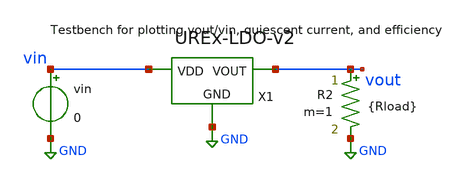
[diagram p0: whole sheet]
** sch_path: xschem/testbenches/VoutvsVin-v2.sch
**.subckt VoutvsVin-v2
vin vin GND 0
R2 vout GND {Rload} m=1
X1 vin vout GND UREx-LDO-v2
**** begin user architecture code



.lib /usr/local/share/pdk/sky130A/libs.tech/ngspice/sky130.lib.spice tt
.param Rload = 20
.dc vin 0.5 5 0.1
*.tran 5u 10m

.control
run
let Rload = 20
let iout = vout/Rload
let iq = (-i(vin))-iout
let eff = (iout*vout*100)/((iout+iq)*vin)

plot v(vout)
plot iq
plot eff

.endc


**** end user architecture code
**.ends

* expanding   symbol:  UREx-LDO-v2.sym # of pins=3
** sym_path: xschem/UREx-LDO-v2.sym
** sch_path: xschem/UREx-LDO-v2.sch
.subckt UREx-LDO-v2 VDD VOUT GND
*.ipin VDD
*.opin VOUT
*.ipin GND
C2 net2 gate 1p m=1
I1 VDD net4 11u
V3 v- GND 0.8
XM10 net3 v- net1 GND sky130_fd_pr__nfet_01v8_lvt L=1 W=0.5 nf=1 ad='int((1 + 1)/2) * 0.5 / 1 * 0.29'
+ as='int((1 + 2)/2) * 0.5 / 1 * 0.29' pd='2*int((1 + 1)/2) * (0.5 / 1 + 0.29)' ps='2*int((1 + 2)/2) * (0.5 / 1 + 0.29)'
+ nrd='0.29 / 0.5 ' nrs='0.29 / 0.5 ' sa=0 sb=0 sd=0 mult=1 m=1
XM11 net2 net3 VDD VDD sky130_fd_pr__pfet_01v8_lvt L=1 W=0.5 nf=1 ad='int((1 + 1)/2) * 0.5 / 1 * 0.29'
+ as='int((1 + 2)/2) * 0.5 / 1 * 0.29' pd='2*int((1 + 1)/2) * (0.5 / 1 + 0.29)' ps='2*int((1 + 2)/2) * (0.5 / 1 + 0.29)'
+ nrd='0.29 / 0.5 ' nrs='0.29 / 0.5 ' sa=0 sb=0 sd=0 mult=1 m=1
XM12 net3 net3 VDD VDD sky130_fd_pr__pfet_01v8_lvt L=1 W=0.5 nf=1 ad='int((1 + 1)/2) * 0.5 / 1 * 0.29'
+ as='int((1 + 2)/2) * 0.5 / 1 * 0.29' pd='2*int((1 + 1)/2) * (0.5 / 1 + 0.29)' ps='2*int((1 + 2)/2) * (0.5 / 1 + 0.29)'
+ nrd='0.29 / 0.5 ' nrs='0.29 / 0.5 ' sa=0 sb=0 sd=0 mult=1 m=1
XM13 net2 v+ net1 GND sky130_fd_pr__nfet_01v8_lvt L=1 W=0.5 nf=1 ad='int((1 + 1)/2) * 0.5 / 1 * 0.29'
+ as='int((1 + 2)/2) * 0.5 / 1 * 0.29' pd='2*int((1 + 1)/2) * (0.5 / 1 + 0.29)' ps='2*int((1 + 2)/2) * (0.5 / 1 + 0.29)'
+ nrd='0.29 / 0.5 ' nrs='0.29 / 0.5 ' sa=0 sb=0 sd=0 mult=1 m=1
XM14 net4 net4 GND GND sky130_fd_pr__nfet_01v8_lvt L=1 W=7 nf=1 ad='int((1 + 1)/2) * 7 / 1 * 0.29' as='int((1 + 2)/2) * 7 / 1 * 0.29'
+ pd='2*int((1 + 1)/2) * (7 / 1 + 0.29)' ps='2*int((1 + 2)/2) * (7 / 1 + 0.29)' nrd='0.29 / 7 ' nrs='0.29 / 7 '
+ sa=0 sb=0 sd=0 mult=1 m=1
XM15 net1 net4 GND GND sky130_fd_pr__nfet_01v8_lvt L=1 W=7 nf=1 ad='int((1 + 1)/2) * 7 / 1 * 0.29' as='int((1 + 2)/2) * 7 / 1 * 0.29'
+ pd='2*int((1 + 1)/2) * (7 / 1 + 0.29)' ps='2*int((1 + 2)/2) * (7 / 1 + 0.29)' nrd='0.29 / 7 ' nrs='0.29 / 7 '
+ sa=0 sb=0 sd=0 mult=1 m=1
XM16 gate net4 GND GND sky130_fd_pr__nfet_01v8_lvt L=0.15 W=27 nf=1 ad='int((1 + 1)/2) * 27 / 1 * 0.29'
+ as='int((1 + 2)/2) * 27 / 1 * 0.29' pd='2*int((1 + 1)/2) * (27 / 1 + 0.29)' ps='2*int((1 + 2)/2) * (27 / 1 + 0.29)'
+ nrd='0.29 / 27 ' nrs='0.29 / 27 ' sa=0 sb=0 sd=0 mult=1 m=1
XM17 gate net2 VDD VDD sky130_fd_pr__pfet_01v8_lvt L=0.35 W=6.3 nf=1 ad='int((1 + 1)/2) * 6.3 / 1 * 0.29'
+ as='int((1 + 2)/2) * 6.3 / 1 * 0.29' pd='2*int((1 + 1)/2) * (6.3 / 1 + 0.29)' ps='2*int((1 + 2)/2) * (6.3 / 1 + 0.29)'
+ nrd='0.29 / 6.3 ' nrs='0.29 / 6.3 ' sa=0 sb=0 sd=0 mult=1 m=1
R3 VOUT v+ 100k m=1
R4 v+ GND 400k m=1
XM1 VOUT gate VDD VDD sky130_fd_pr__pfet_01v8_lvt L=0.35 W=35 nf=1 ad='int((1 + 1)/2) * 35 / 1 * 0.29'
+ as='int((1 + 2)/2) * 35 / 1 * 0.29' pd='2*int((1 + 1)/2) * (35 / 1 + 0.29)' ps='2*int((1 + 2)/2) * (35 / 1 + 0.29)'
+ nrd='0.29 / 35 ' nrs='0.29 / 35 ' sa=0 sb=0 sd=0 mult=408 m=408
.ends

.GLOBAL GND
.end
